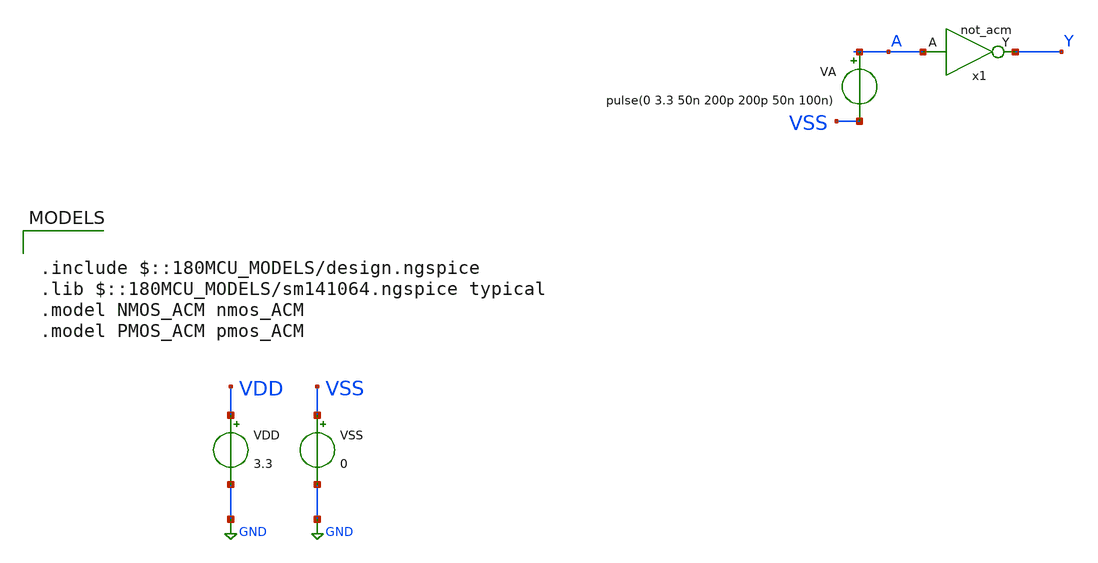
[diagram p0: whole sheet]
** sch_path: legacy/Examples/IHP-SG13/xschem/TB_not_acm.sch
* legacy/Examples/IHP-SG13/xschem/symbol/not_acm.sym:
* Copyright 2022 Stefan Frederik Schippers
* Licensed under the Apache License, Version 2.0 (the "License");
**.subckt TB_not_acm
VA A VSS pulse(0 3.3 50n 200p 200p 50n 100n)
VDD VDD GND 3.3
VSS VSS GND 0
x1 A Y VDD VSS not_acm
**** begin user architecture code

.include $::180MCU_MODELS/design.ngspice
.lib $::180MCU_MODELS/sm141064.ngspice typical
.model NMOS_ACM nmos_ACM
.model PMOS_ACM pmos_ACM



.option gmin=1e-15

.control
pre_osdi ./NMOS_ACM_2V0.osdi
pre_osdi ./PMOS_ACM_2V0.osdi
save all


tran 1n 500n
remzerovec
write TB_not_acm.raw
set appendwrite

.endc


**** end user architecture code
**.ends

* expanding   symbol:  symbol/not_acm.sym # of pins=2
** sym_path: legacy/Examples/IHP-SG13/xschem/symbol/not_acm.sym
** sch_path: legacy/Examples/IHP-SG13/xschem/symbol/not_acm.sch
.subckt not_acm A Y VDDPIN VSSPIN
*.ipin A
*.opin Y
N1 Y A VSSPIN VSSPIN NMOS_ACM w=2u l=2u n=1.38 is=67.3n vt0=0.652 sigma=20m zeta=5m
N2 Y A VDDPIN VDDPIN PMOS_ACM w=2u l=2u n=1.438 is=17.94n vt0=0.7774 sigma=20m zeta=5m
.ends

.GLOBAL GND
.end
